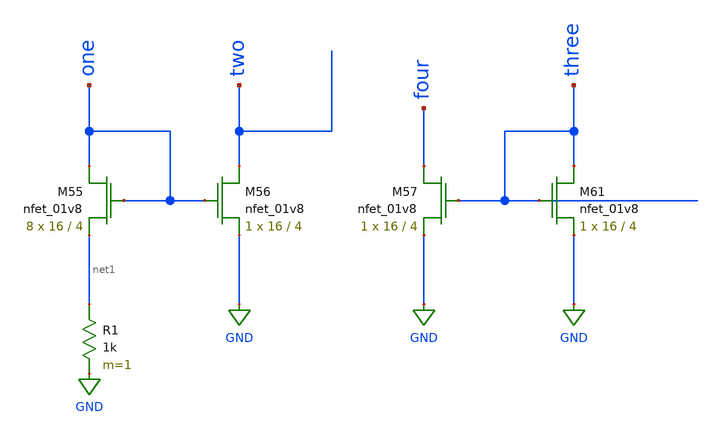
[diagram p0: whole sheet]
** sch_path: schematic/LDS/test/test/test2.sch
**.subckt test2
XM55 one one net1 GND sky130_fd_pr__nfet_01v8 L=4 W=16 nf=1 ad='int((nf+1)/2) * W/nf * 0.29' as='int((nf+2)/2) * W/nf * 0.29'
+ pd='2*int((nf+1)/2) * (W/nf + 0.29)' ps='2*int((nf+2)/2) * (W/nf + 0.29)' nrd='0.29 / W' nrs='0.29 / W'
+ sa=0 sb=0 sd=0 mult=8 m=8
XM56 two one GND GND sky130_fd_pr__nfet_01v8 L=4 W=16 nf=1 ad='int((nf+1)/2) * W/nf * 0.29' as='int((nf+2)/2) * W/nf * 0.29'
+ pd='2*int((nf+1)/2) * (W/nf + 0.29)' ps='2*int((nf+2)/2) * (W/nf + 0.29)' nrd='0.29 / W' nrs='0.29 / W'
+ sa=0 sb=0 sd=0 mult=1 m=1
XM57 four three GND GND sky130_fd_pr__nfet_01v8 L=4 W=16 nf=1 ad='int((nf+1)/2) * W/nf * 0.29' as='int((nf+2)/2) * W/nf * 0.29'
+ pd='2*int((nf+1)/2) * (W/nf + 0.29)' ps='2*int((nf+2)/2) * (W/nf + 0.29)' nrd='0.29 / W' nrs='0.29 / W'
+ sa=0 sb=0 sd=0 mult=1 m=1
XM61 three three GND GND sky130_fd_pr__nfet_01v8 L=4 W=16 nf=1 ad='int((nf+1)/2) * W/nf * 0.29' as='int((nf+2)/2) * W/nf * 0.29'
+ pd='2*int((nf+1)/2) * (W/nf + 0.29)' ps='2*int((nf+2)/2) * (W/nf + 0.29)' nrd='0.29 / W' nrs='0.29 / W'
+ sa=0 sb=0 sd=0 mult=1 m=1
R1 net1 GND 1k m=1
**.ends
.GLOBAL GND
.end
